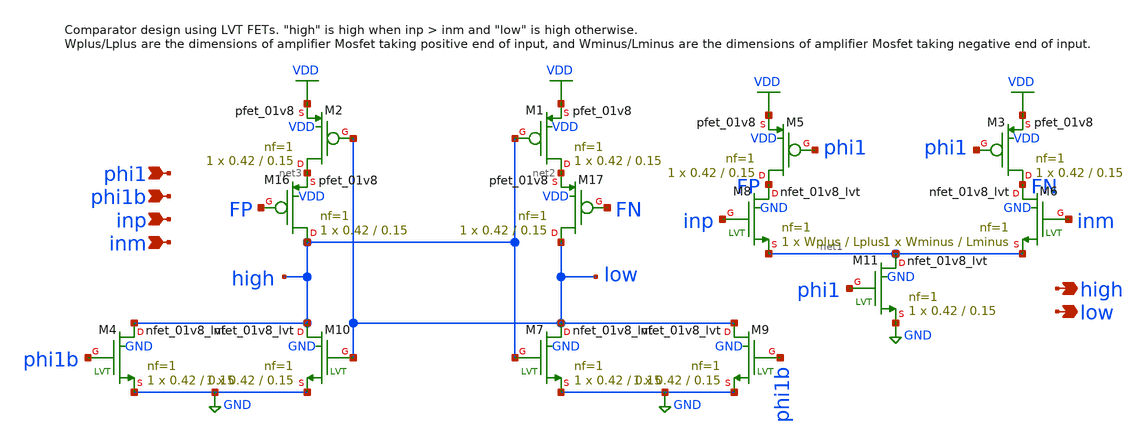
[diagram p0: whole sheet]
** sch_path: xschem/archive/comparator_latest/comparator_single_tail.sch
**.subckt comparator_single_tail phi1 high phi1b inp inm low
*.ipin phi1
*.opin high
*.ipin phi1b
*.ipin inp
*.ipin inm
*.opin low
XM1 net2 high VDD VDD sky130_fd_pr__pfet_01v8 L=0.15 W=0.42 nf=1 ad='int((nf+1)/2) * W/nf * 0.29' as='int((nf+2)/2) * W/nf * 0.29'
+ pd='2*int((nf+1)/2) * (W/nf + 0.29)' ps='2*int((nf+2)/2) * (W/nf + 0.29)' nrd='0.29 / W' nrs='0.29 / W'
+ sa=0 sb=0 sd=0 mult=1 m=1
XM2 net3 low VDD VDD sky130_fd_pr__pfet_01v8 L=0.15 W=0.42 nf=1 ad='int((nf+1)/2) * W/nf * 0.29' as='int((nf+2)/2) * W/nf * 0.29'
+ pd='2*int((nf+1)/2) * (W/nf + 0.29)' ps='2*int((nf+2)/2) * (W/nf + 0.29)' nrd='0.29 / W' nrs='0.29 / W'
+ sa=0 sb=0 sd=0 mult=1 m=1
XM16 high FP net3 VDD sky130_fd_pr__pfet_01v8 L=0.15 W=0.42 nf=1 ad='int((nf+1)/2) * W/nf * 0.29' as='int((nf+2)/2) * W/nf * 0.29'
+ pd='2*int((nf+1)/2) * (W/nf + 0.29)' ps='2*int((nf+2)/2) * (W/nf + 0.29)' nrd='0.29 / W' nrs='0.29 / W'
+ sa=0 sb=0 sd=0 mult=1 m=1
XM17 low FN net2 VDD sky130_fd_pr__pfet_01v8 L=0.15 W=0.42 nf=1 ad='int((nf+1)/2) * W/nf * 0.29' as='int((nf+2)/2) * W/nf * 0.29'
+ pd='2*int((nf+1)/2) * (W/nf + 0.29)' ps='2*int((nf+2)/2) * (W/nf + 0.29)' nrd='0.29 / W' nrs='0.29 / W'
+ sa=0 sb=0 sd=0 mult=1 m=1
XM3 FN phi1 VDD VDD sky130_fd_pr__pfet_01v8 L=0.15 W=0.42 nf=1 ad='int((nf+1)/2) * W/nf * 0.29' as='int((nf+2)/2) * W/nf * 0.29'
+ pd='2*int((nf+1)/2) * (W/nf + 0.29)' ps='2*int((nf+2)/2) * (W/nf + 0.29)' nrd='0.29 / W' nrs='0.29 / W'
+ sa=0 sb=0 sd=0 mult=1 m=1
XM5 FP phi1 VDD VDD sky130_fd_pr__pfet_01v8 L=0.15 W=0.42 nf=1 ad='int((nf+1)/2) * W/nf * 0.29' as='int((nf+2)/2) * W/nf * 0.29'
+ pd='2*int((nf+1)/2) * (W/nf + 0.29)' ps='2*int((nf+2)/2) * (W/nf + 0.29)' nrd='0.29 / W' nrs='0.29 / W'
+ sa=0 sb=0 sd=0 mult=1 m=1
XM4 high phi1b GND GND sky130_fd_pr__nfet_01v8_lvt L=0.15 W=0.42 nf=1 ad='int((nf+1)/2) * W/nf * 0.29'
+ as='int((nf+2)/2) * W/nf * 0.29' pd='2*int((nf+1)/2) * (W/nf + 0.29)' ps='2*int((nf+2)/2) * (W/nf + 0.29)'
+ nrd='0.29 / W' nrs='0.29 / W' sa=0 sb=0 sd=0 mult=1 m=1
XM7 low high GND GND sky130_fd_pr__nfet_01v8_lvt L=0.15 W=0.42 nf=1 ad='int((nf+1)/2) * W/nf * 0.29'
+ as='int((nf+2)/2) * W/nf * 0.29' pd='2*int((nf+1)/2) * (W/nf + 0.29)' ps='2*int((nf+2)/2) * (W/nf + 0.29)'
+ nrd='0.29 / W' nrs='0.29 / W' sa=0 sb=0 sd=0 mult=1 m=1
XM8 FP inp net1 GND sky130_fd_pr__nfet_01v8_lvt L=Lplus W=Wplus nf=1 ad='int((nf+1)/2) * W/nf * 0.29'
+ as='int((nf+2)/2) * W/nf * 0.29' pd='2*int((nf+1)/2) * (W/nf + 0.29)' ps='2*int((nf+2)/2) * (W/nf + 0.29)'
+ nrd='0.29 / W' nrs='0.29 / W' sa=0 sb=0 sd=0 mult=1 m=1
XM6 FN inm net1 GND sky130_fd_pr__nfet_01v8_lvt L=Lminus W=Wminus nf=1 ad='int((nf+1)/2) * W/nf * 0.29'
+ as='int((nf+2)/2) * W/nf * 0.29' pd='2*int((nf+1)/2) * (W/nf + 0.29)' ps='2*int((nf+2)/2) * (W/nf + 0.29)'
+ nrd='0.29 / W' nrs='0.29 / W' sa=0 sb=0 sd=0 mult=1 m=1
XM9 low phi1b GND GND sky130_fd_pr__nfet_01v8_lvt L=0.15 W=0.42 nf=1 ad='int((nf+1)/2) * W/nf * 0.29'
+ as='int((nf+2)/2) * W/nf * 0.29' pd='2*int((nf+1)/2) * (W/nf + 0.29)' ps='2*int((nf+2)/2) * (W/nf + 0.29)'
+ nrd='0.29 / W' nrs='0.29 / W' sa=0 sb=0 sd=0 mult=1 m=1
XM10 high low GND GND sky130_fd_pr__nfet_01v8_lvt L=0.15 W=0.42 nf=1 ad='int((nf+1)/2) * W/nf * 0.29'
+ as='int((nf+2)/2) * W/nf * 0.29' pd='2*int((nf+1)/2) * (W/nf + 0.29)' ps='2*int((nf+2)/2) * (W/nf + 0.29)'
+ nrd='0.29 / W' nrs='0.29 / W' sa=0 sb=0 sd=0 mult=1 m=1
XM11 net1 phi1 GND GND sky130_fd_pr__nfet_01v8_lvt L=0.15 W=0.42 nf=1 ad='int((nf+1)/2) * W/nf * 0.29'
+ as='int((nf+2)/2) * W/nf * 0.29' pd='2*int((nf+1)/2) * (W/nf + 0.29)' ps='2*int((nf+2)/2) * (W/nf + 0.29)'
+ nrd='0.29 / W' nrs='0.29 / W' sa=0 sb=0 sd=0 mult=1 m=1
**.ends
.GLOBAL VDD
.GLOBAL GND
.end
